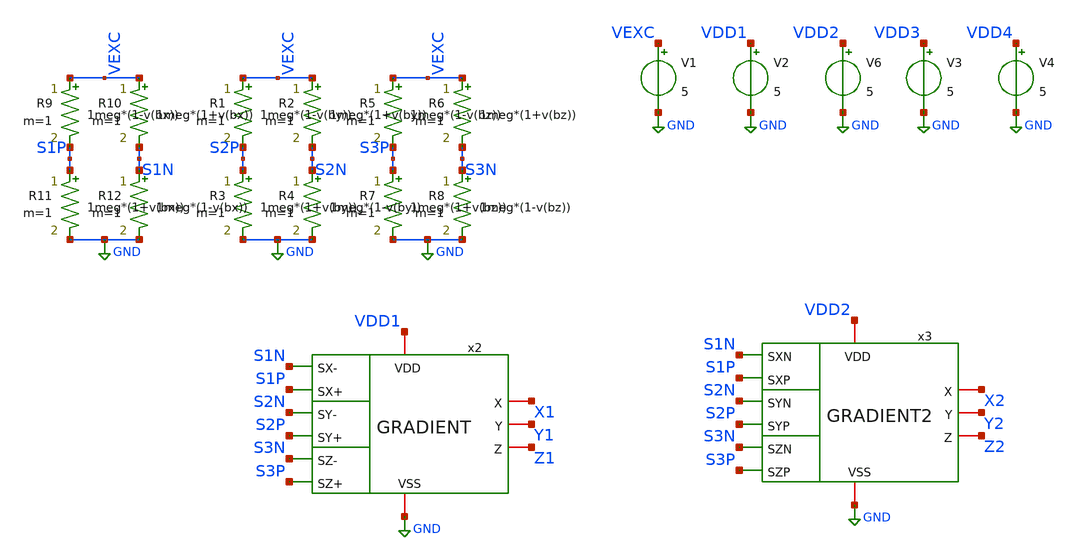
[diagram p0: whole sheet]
** sch_path: FINAL/XSCHEM/TEST_TOTAL/test_GRADIENT.sch
**.subckt test_GRADIENT
V1 VEXC GND 5
V2 VDD1 GND 5
V6 VDD2 GND 5
x2 S1N S1P VDD1 X1 S2N Y1 Z1 S2P GND S3N S3P GRADIENT
x3 S1N S1P VDD2 X2 S2N Y2 Z2 S2P GND S3N S3P GRADIENT2
R1 VEXC S2P r=' 1meg*(1-v(by)) '
R2 VEXC S2N r=' 1meg*(1+v(by)) '
R3 S2P GND r=' 1meg*(1+v(by)) '
R4 S2N GND r=' 1meg*(1-v(by)) '
V3 VDD3 GND 5
V4 VDD4 GND 5
R5 VEXC S3P r=' 1meg*(1-v(bz)) '
R6 VEXC S3N r=' 1meg*(1+v(bz)) '
R7 S3P GND r=' 1meg*(1+v(bz)) '
R8 S3N GND r=' 1meg*(1-v(bz)) '
R9 VEXC S1P r=' 1meg*(1-v(bx)) '
R10 VEXC S1N r=' 1meg*(1+v(bx)) '
R11 S1P GND r=' 1meg*(1+v(bx)) '
R12 S1N GND r=' 1meg*(1-v(bx)) '
**** begin user architecture code

.include $::180MCU_MODELS/design.ngspice
.lib $::180MCU_MODELS/sm141064.ngspice typical
.lib $::180MCU_MODELS/sm141064.ngspice cap_mim
.lib $::180MCU_MODELS/sm141064.ngspice res_typical
.lib $::180MCU_MODELS/sm141064.ngspice moscap_typical
.lib $::180MCU_MODELS/sm141064.ngspice mimcap_typical



* THE FIELD. Three components 120 degrees apart, which is what makes them sum
* to zero: the vector only changes DIRECTION, not magnitude. Sweeping
* Vang from 0 to 360 covers the whole circle, and if the chain is right each
* eje deberia ganar exactamente 120 grados: X de -60 a 60, Y de 60 a 180 y Z de
* 180 to 300. How far those three boundaries drift is the figure of the bench.
*
* v(amp) IS dR/R, with no conversion factors in between: each bridge arm is
* 1meg*(1 +- v(bx)), so the amplifier sees VEXC*v(bx) of differential signal
* and the common mode stays pinned at VEXC/2 whatever happens to
* la senal. Eso segundo no es un adorno: si el modo comun se moviera con la
* signal it would mix with these cells' common-mode sensitivity and there
* would be no way to separate the two when reading the curve.
*
* Va con fuentes B y resistencias de comportamiento, y no barriendo
* resistors, because dc takes two nested sources at most and here there are
* TWELVE resistors that must all move at once and consistently.
*
* AND A SECOND MODE, for the octant cases. The rotation above pins the three
* readings to bx+by+bz = 0, so patterns like (+,+,+) are unreachable by
* construction and this bench can only ever see three of the eight sign
* combinations. With v(sel) = 1 each reading becomes v(amp) times its own
* coefficient cx/cy/cz, so the SIGNS of those three coefficients pick the
* octant and their MAGNITUDES pick the ordering, while sweeping Vamp still
* sweeps the field inside that octant.
*
* The decoder puts out the SMALLEST axis (X = XY*XZ), so the expected answer
* at every point is argmin(cx, cy, cz) -- a truth table checkable entry by
* entry. Coefficients are given distinct magnitudes on purpose: three equal
* ones are a three-way tie with no right answer.
*
* v(sel) = 0 leaves the rotation exactly as it was: nothing above changes.
Vamp amp 0 0.02
Vang ang 0 0
Vsel sel 0 0
Vcx cx 0 1
Vcy cy 0 0
Vcz cz 0 0
Bbx bx 0 v='v(sel) > 0.5 ? v(amp)*v(cx) : v(amp)*cos( v(ang)       *3.14159265358979/180)'
Bby by 0 v='v(sel) > 0.5 ? v(amp)*v(cy) : v(amp)*cos((v(ang)-120.0)*3.14159265358979/180)'
Bbz bz 0 v='v(sel) > 0.5 ? v(amp)*v(cz) : v(amp)*cos((v(ang)+120.0)*3.14159265358979/180)'




* THE SAME TWO CHAINS, REBUILT FROM THE v2 LAYOUT BLOCKS.
* They hang off the SAME six sensor nodes as the schematic ones and each
* carries its own supply, so current draw can be compared too.
*
* La topologia es la de COMBINATION/GRADIENT.sch, copiada nodo a nodo:
*
*     amp X: S1N->INN  S1P->INP  -> SX        COMP XY: INN=SX INP=SY -> XY
*     amp Y: S2N->INN  S2P->INP  -> SY        COMP XZ: INN=SX INP=SZ -> XZ
*     amp Z: S3N->INN  S3P->INP  -> SZ        COMP YZ: INN=SY INP=SZ -> YZ
*                                             DECODER: XY XZ YZ -> X Y Z
*
* CAREFUL WITH THE PORT ORDER. xschem emits them in the order of the symbol B
* lines and magic in the order it finds them in the layout, and they do NOT agree:
* el esquematico declara OPAM VDD INN OUT INP VSS y el extraido OPAM VSS VDD OUT
* INP INN. Cablear las dos igual significa cosas distintas y no da ningun error.
* That is why the real order is written above each group, and why the files are
* the _V2_ ones produced by TEST/preparar_extraidos.sh: it renames the subcircuit
* -- both declare the same name and cannot be included together -- and normalises
* the order. Note that OPAM_LIN_flat has OUT in the middle and the others do not.
.include ../../../../layouts_v2/OPAM/mag/OPAM_V2_pex_rc.spice
.include ../../../../layouts_v2/OPAM_LIN_flat/mag/OPAM_LIN_flat_V2_pex_rc.spice
.include ../../../../layouts_v2/COMP/mag/COMP_V2_pex_rc.spice
.include ../../../../layouts_v2/DECODER/mag/DECODER_V2_pex_rc.spice

* --- G3: the G1 chain, with the v2 layout OPAM
* .subckt OPAM_V2     VSS VDD OUT INP INN
XA31 GND VDD3 SX3 S1P S1N OPAM_V2
XA32 GND VDD3 SY3 S2P S2N OPAM_V2
XA33 GND VDD3 SZ3 S3P S3N OPAM_V2
* .subckt COMP_V2     VSS VDD OUT INP INN
XC31 GND VDD3 XY3 SY3 SX3 COMP_V2
XC32 GND VDD3 XZ3 SZ3 SX3 COMP_V2
XC33 GND VDD3 YZ3 SZ3 SY3 COMP_V2
* .subckt DECODER_V2  VSS VDD YZ Z XY XZ Y X
XD3  GND VDD3 YZ3 Z3 XY3 XZ3 Y3 X3 DECODER_V2

* --- G4: the G2 chain, with the v2 layout OPAM_LIN_flat
* .subckt OPAM_LIN_flat_V2  VSS VDD INP OUT INN
XA41 GND VDD4 S1P SX4 S1N OPAM_LIN_flat_V2
XA42 GND VDD4 S2P SY4 S2N OPAM_LIN_flat_V2
XA43 GND VDD4 S3P SZ4 S3N OPAM_LIN_flat_V2
* .subckt COMP_V2     VSS VDD OUT INP INN
XC41 GND VDD4 XY4 SY4 SX4 COMP_V2
XC42 GND VDD4 XZ4 SZ4 SX4 COMP_V2
XC43 GND VDD4 YZ4 SZ4 SY4 COMP_V2
* .subckt DECODER_V2  VSS VDD YZ Z XY XZ Y X
XD4  GND VDD4 YZ4 Z4 XY4 XZ4 Y4 X4 DECODER_V2




* CAREFUL: not one brace in this text. xschem counts them to find where the
* attribute block ends and a single one inside a comment cuts it in half,
* leaving the netlist with the template 'blabla' and raising no error.
*
* This bench does NOT need a common-mode source, unlike test_comp_* and
* test_opam_*: there the input pair were two gates with no DC path to
* ground, and here the bridge itself provides it.
*
* The intermediate signals of the schematic chains come out by hierarchical
* name, v(x2.SX) and company. In the hand-rebuilt ones the nodes are
* primer nivel y se llaman SX3, XY3 y asi.
.save all
.control
* Fondo de escala de una AMR tipica: dR/R = 2 %, o sea 100 mV diferenciales.
alter Vamp = 0.02
dc Vang 0 360 0.5
wrdata ancho.txt v(X1) v(Y1) v(Z1) v(X2) v(Y2) v(Z2) v(X3) v(Y3) v(Z3) v(X4) v(Y4) v(Z4) v(x2.SX) v(x2.SY) v(x2.SZ) v(x3.SX) v(x3.SY) v(x3.SZ) v(SX3) v(SY3) v(SZ3) v(SX4) v(SY4) v(SZ4) v(x2.net1) v(x2.net2) v(x2.net3) v(x3.net1) v(x3.net2) v(x3.net3) v(XY3) v(XZ3) v(YZ3) v(XY4) v(XZ4) v(YZ4) v(S1P) v(S1N) v(S2P) v(S2N) v(S3P) v(S3N) v(VEXC)*i(V1) v(VDD1)*i(V2) v(VDD2)*i(V6) v(VDD3)*i(V3) v(VDD4)*i(V4)
* Ventana fina: dR/R = 50 ppm, o sea 250 uV diferenciales.
alter Vamp = 50u
dc Vang 0 360 0.5
wrdata fino.txt v(X1) v(Y1) v(Z1) v(X2) v(Y2) v(Z2) v(X3) v(Y3) v(Z3) v(X4) v(Y4) v(Z4) v(x2.SX) v(x2.SY) v(x2.SZ) v(x3.SX) v(x3.SY) v(x3.SZ) v(SX3) v(SY3) v(SZ3) v(SX4) v(SY4) v(SZ4) v(x2.net1) v(x2.net2) v(x2.net3) v(x3.net1) v(x3.net2) v(x3.net3) v(XY3) v(XZ3) v(YZ3) v(XY4) v(XZ4) v(YZ4) v(S1P) v(S1N) v(S2P) v(S2N) v(S3P) v(S3N) v(VEXC)*i(V1) v(VDD1)*i(V2) v(VDD2)*i(V6) v(VDD3)*i(V3) v(VDD4)*i(V4)
* --------------------------------------------------------------------------
* FIELD SWEEP. Everything above turns the field and keeps its size; these two
* do the opposite -- hold the direction and sweep the MAGNITUDE, which is the
* axis a real magnet moves along as you walk towards it.
*
* The angle is parked at 60 deg, the middle of a sector: on a boundary the
* decision is meant to be undefined and the sweep would only measure noise.
*
* AND THE SWEEP DOES NOT START AT ZERO. With Vamp = 0 the three bridges are
* identical, so the three amplifiers sit at the same output and all three
* comparators land exactly on their trip point: the operating point is not
* unique and ngspice spends the sweep in gmin stepping. Starting one step in
* costs nothing and the solution is definite everywhere.
*
* Only the linear-amplifier chain, G2 (schematic) and G4 (layout), and their
* own new files so ancho.txt and fino.txt keep the column order analizar.py
* reads.
alter Vang = 60
dc Vamp 20u 0.02 20u
wrdata campo.txt v(S1P) v(S1N) v(S2P) v(S2N) v(S3P) v(S3N)  v(x3.SX) v(x3.SY) v(x3.SZ) v(x3.net1) v(x3.net2) v(x3.net3)  v(X2) v(Y2) v(Z2)  v(SX4) v(SY4) v(SZ4) v(XY4) v(XZ4) v(YZ4)  v(X4) v(Y4) v(Z4)  v(VDD2)*i(V6) v(VDD4)*i(V4)
* And the low end on its own scale, where the offsets and the noise live.
dc Vamp 1u 1m 1u
wrdata campo_fino.txt v(S1P) v(S1N) v(S2P) v(S2N) v(S3P) v(S3N)  v(x3.SX) v(x3.SY) v(x3.SZ) v(x3.net1) v(x3.net2) v(x3.net3)  v(X2) v(Y2) v(Z2)  v(SX4) v(SY4) v(SZ4) v(XY4) v(XZ4) v(YZ4)  v(X4) v(Y4) v(Z4)  v(VDD2)*i(V6) v(VDD4)*i(V4)
* --------------------------------------------------------------------------
* OCTANT CASES. Eight sign patterns times three magnitude orderings, so
* every axis gets to be the smallest, the middle one and the largest in
* each octant: 24 cases. The coefficients are written into the file as
* its first three vectors, so each file says which case it is and no
* separate manifest can drift out of step with it.
alter Vsel = 1
* case 01: c = (+1.0, +0.6, +0.3)  ->  expected Z
alter Vcx = 1.0
alter Vcy = 0.6
alter Vcz = 0.3
dc Vamp 200u 0.02 200u
wrdata oct_01.txt v(cx) v(cy) v(cz) v(S1P) v(S1N) v(S2P) v(S2N) v(S3P) v(S3N)  v(x3.SX) v(x3.SY) v(x3.SZ) v(x3.net1) v(x3.net2) v(x3.net3)  v(X2) v(Y2) v(Z2)  v(SX4) v(SY4) v(SZ4) v(XY4) v(XZ4) v(YZ4)  v(X4) v(Y4) v(Z4)
* case 02: c = (+0.3, +1.0, +0.6)  ->  expected X
alter Vcx = 0.3
alter Vcy = 1.0
alter Vcz = 0.6
dc Vamp 200u 0.02 200u
wrdata oct_02.txt v(cx) v(cy) v(cz) v(S1P) v(S1N) v(S2P) v(S2N) v(S3P) v(S3N)  v(x3.SX) v(x3.SY) v(x3.SZ) v(x3.net1) v(x3.net2) v(x3.net3)  v(X2) v(Y2) v(Z2)  v(SX4) v(SY4) v(SZ4) v(XY4) v(XZ4) v(YZ4)  v(X4) v(Y4) v(Z4)
* case 03: c = (+0.6, +0.3, +1.0)  ->  expected Y
alter Vcx = 0.6
alter Vcy = 0.3
alter Vcz = 1.0
dc Vamp 200u 0.02 200u
wrdata oct_03.txt v(cx) v(cy) v(cz) v(S1P) v(S1N) v(S2P) v(S2N) v(S3P) v(S3N)  v(x3.SX) v(x3.SY) v(x3.SZ) v(x3.net1) v(x3.net2) v(x3.net3)  v(X2) v(Y2) v(Z2)  v(SX4) v(SY4) v(SZ4) v(XY4) v(XZ4) v(YZ4)  v(X4) v(Y4) v(Z4)
* case 04: c = (+1.0, +0.6, -0.3)  ->  expected Z
alter Vcx = 1.0
alter Vcy = 0.6
alter Vcz = -0.3
dc Vamp 200u 0.02 200u
wrdata oct_04.txt v(cx) v(cy) v(cz) v(S1P) v(S1N) v(S2P) v(S2N) v(S3P) v(S3N)  v(x3.SX) v(x3.SY) v(x3.SZ) v(x3.net1) v(x3.net2) v(x3.net3)  v(X2) v(Y2) v(Z2)  v(SX4) v(SY4) v(SZ4) v(XY4) v(XZ4) v(YZ4)  v(X4) v(Y4) v(Z4)
* case 05: c = (+0.3, +1.0, -0.6)  ->  expected Z
alter Vcx = 0.3
alter Vcy = 1.0
alter Vcz = -0.6
dc Vamp 200u 0.02 200u
wrdata oct_05.txt v(cx) v(cy) v(cz) v(S1P) v(S1N) v(S2P) v(S2N) v(S3P) v(S3N)  v(x3.SX) v(x3.SY) v(x3.SZ) v(x3.net1) v(x3.net2) v(x3.net3)  v(X2) v(Y2) v(Z2)  v(SX4) v(SY4) v(SZ4) v(XY4) v(XZ4) v(YZ4)  v(X4) v(Y4) v(Z4)
* case 06: c = (+0.6, +0.3, -1.0)  ->  expected Z
alter Vcx = 0.6
alter Vcy = 0.3
alter Vcz = -1.0
dc Vamp 200u 0.02 200u
wrdata oct_06.txt v(cx) v(cy) v(cz) v(S1P) v(S1N) v(S2P) v(S2N) v(S3P) v(S3N)  v(x3.SX) v(x3.SY) v(x3.SZ) v(x3.net1) v(x3.net2) v(x3.net3)  v(X2) v(Y2) v(Z2)  v(SX4) v(SY4) v(SZ4) v(XY4) v(XZ4) v(YZ4)  v(X4) v(Y4) v(Z4)
* case 07: c = (+1.0, -0.6, +0.3)  ->  expected Y
alter Vcx = 1.0
alter Vcy = -0.6
alter Vcz = 0.3
dc Vamp 200u 0.02 200u
wrdata oct_07.txt v(cx) v(cy) v(cz) v(S1P) v(S1N) v(S2P) v(S2N) v(S3P) v(S3N)  v(x3.SX) v(x3.SY) v(x3.SZ) v(x3.net1) v(x3.net2) v(x3.net3)  v(X2) v(Y2) v(Z2)  v(SX4) v(SY4) v(SZ4) v(XY4) v(XZ4) v(YZ4)  v(X4) v(Y4) v(Z4)
* case 08: c = (+0.3, -1.0, +0.6)  ->  expected Y
alter Vcx = 0.3
alter Vcy = -1.0
alter Vcz = 0.6
dc Vamp 200u 0.02 200u
wrdata oct_08.txt v(cx) v(cy) v(cz) v(S1P) v(S1N) v(S2P) v(S2N) v(S3P) v(S3N)  v(x3.SX) v(x3.SY) v(x3.SZ) v(x3.net1) v(x3.net2) v(x3.net3)  v(X2) v(Y2) v(Z2)  v(SX4) v(SY4) v(SZ4) v(XY4) v(XZ4) v(YZ4)  v(X4) v(Y4) v(Z4)
* case 09: c = (+0.6, -0.3, +1.0)  ->  expected Y
alter Vcx = 0.6
alter Vcy = -0.3
alter Vcz = 1.0
dc Vamp 200u 0.02 200u
wrdata oct_09.txt v(cx) v(cy) v(cz) v(S1P) v(S1N) v(S2P) v(S2N) v(S3P) v(S3N)  v(x3.SX) v(x3.SY) v(x3.SZ) v(x3.net1) v(x3.net2) v(x3.net3)  v(X2) v(Y2) v(Z2)  v(SX4) v(SY4) v(SZ4) v(XY4) v(XZ4) v(YZ4)  v(X4) v(Y4) v(Z4)
* case 10: c = (+1.0, -0.6, -0.3)  ->  expected Y
alter Vcx = 1.0
alter Vcy = -0.6
alter Vcz = -0.3
dc Vamp 200u 0.02 200u
wrdata oct_10.txt v(cx) v(cy) v(cz) v(S1P) v(S1N) v(S2P) v(S2N) v(S3P) v(S3N)  v(x3.SX) v(x3.SY) v(x3.SZ) v(x3.net1) v(x3.net2) v(x3.net3)  v(X2) v(Y2) v(Z2)  v(SX4) v(SY4) v(SZ4) v(XY4) v(XZ4) v(YZ4)  v(X4) v(Y4) v(Z4)
* case 11: c = (+0.3, -1.0, -0.6)  ->  expected Y
alter Vcx = 0.3
alter Vcy = -1.0
alter Vcz = -0.6
dc Vamp 200u 0.02 200u
wrdata oct_11.txt v(cx) v(cy) v(cz) v(S1P) v(S1N) v(S2P) v(S2N) v(S3P) v(S3N)  v(x3.SX) v(x3.SY) v(x3.SZ) v(x3.net1) v(x3.net2) v(x3.net3)  v(X2) v(Y2) v(Z2)  v(SX4) v(SY4) v(SZ4) v(XY4) v(XZ4) v(YZ4)  v(X4) v(Y4) v(Z4)
* case 12: c = (+0.6, -0.3, -1.0)  ->  expected Z
alter Vcx = 0.6
alter Vcy = -0.3
alter Vcz = -1.0
dc Vamp 200u 0.02 200u
wrdata oct_12.txt v(cx) v(cy) v(cz) v(S1P) v(S1N) v(S2P) v(S2N) v(S3P) v(S3N)  v(x3.SX) v(x3.SY) v(x3.SZ) v(x3.net1) v(x3.net2) v(x3.net3)  v(X2) v(Y2) v(Z2)  v(SX4) v(SY4) v(SZ4) v(XY4) v(XZ4) v(YZ4)  v(X4) v(Y4) v(Z4)
* case 13: c = (-1.0, +0.6, +0.3)  ->  expected X
alter Vcx = -1.0
alter Vcy = 0.6
alter Vcz = 0.3
dc Vamp 200u 0.02 200u
wrdata oct_13.txt v(cx) v(cy) v(cz) v(S1P) v(S1N) v(S2P) v(S2N) v(S3P) v(S3N)  v(x3.SX) v(x3.SY) v(x3.SZ) v(x3.net1) v(x3.net2) v(x3.net3)  v(X2) v(Y2) v(Z2)  v(SX4) v(SY4) v(SZ4) v(XY4) v(XZ4) v(YZ4)  v(X4) v(Y4) v(Z4)
* case 14: c = (-0.3, +1.0, +0.6)  ->  expected X
alter Vcx = -0.3
alter Vcy = 1.0
alter Vcz = 0.6
dc Vamp 200u 0.02 200u
wrdata oct_14.txt v(cx) v(cy) v(cz) v(S1P) v(S1N) v(S2P) v(S2N) v(S3P) v(S3N)  v(x3.SX) v(x3.SY) v(x3.SZ) v(x3.net1) v(x3.net2) v(x3.net3)  v(X2) v(Y2) v(Z2)  v(SX4) v(SY4) v(SZ4) v(XY4) v(XZ4) v(YZ4)  v(X4) v(Y4) v(Z4)
* case 15: c = (-0.6, +0.3, +1.0)  ->  expected X
alter Vcx = -0.6
alter Vcy = 0.3
alter Vcz = 1.0
dc Vamp 200u 0.02 200u
wrdata oct_15.txt v(cx) v(cy) v(cz) v(S1P) v(S1N) v(S2P) v(S2N) v(S3P) v(S3N)  v(x3.SX) v(x3.SY) v(x3.SZ) v(x3.net1) v(x3.net2) v(x3.net3)  v(X2) v(Y2) v(Z2)  v(SX4) v(SY4) v(SZ4) v(XY4) v(XZ4) v(YZ4)  v(X4) v(Y4) v(Z4)
* case 16: c = (-1.0, +0.6, -0.3)  ->  expected X
alter Vcx = -1.0
alter Vcy = 0.6
alter Vcz = -0.3
dc Vamp 200u 0.02 200u
wrdata oct_16.txt v(cx) v(cy) v(cz) v(S1P) v(S1N) v(S2P) v(S2N) v(S3P) v(S3N)  v(x3.SX) v(x3.SY) v(x3.SZ) v(x3.net1) v(x3.net2) v(x3.net3)  v(X2) v(Y2) v(Z2)  v(SX4) v(SY4) v(SZ4) v(XY4) v(XZ4) v(YZ4)  v(X4) v(Y4) v(Z4)
* case 17: c = (-0.3, +1.0, -0.6)  ->  expected Z
alter Vcx = -0.3
alter Vcy = 1.0
alter Vcz = -0.6
dc Vamp 200u 0.02 200u
wrdata oct_17.txt v(cx) v(cy) v(cz) v(S1P) v(S1N) v(S2P) v(S2N) v(S3P) v(S3N)  v(x3.SX) v(x3.SY) v(x3.SZ) v(x3.net1) v(x3.net2) v(x3.net3)  v(X2) v(Y2) v(Z2)  v(SX4) v(SY4) v(SZ4) v(XY4) v(XZ4) v(YZ4)  v(X4) v(Y4) v(Z4)
* case 18: c = (-0.6, +0.3, -1.0)  ->  expected Z
alter Vcx = -0.6
alter Vcy = 0.3
alter Vcz = -1.0
dc Vamp 200u 0.02 200u
wrdata oct_18.txt v(cx) v(cy) v(cz) v(S1P) v(S1N) v(S2P) v(S2N) v(S3P) v(S3N)  v(x3.SX) v(x3.SY) v(x3.SZ) v(x3.net1) v(x3.net2) v(x3.net3)  v(X2) v(Y2) v(Z2)  v(SX4) v(SY4) v(SZ4) v(XY4) v(XZ4) v(YZ4)  v(X4) v(Y4) v(Z4)
* case 19: c = (-1.0, -0.6, +0.3)  ->  expected X
alter Vcx = -1.0
alter Vcy = -0.6
alter Vcz = 0.3
dc Vamp 200u 0.02 200u
wrdata oct_19.txt v(cx) v(cy) v(cz) v(S1P) v(S1N) v(S2P) v(S2N) v(S3P) v(S3N)  v(x3.SX) v(x3.SY) v(x3.SZ) v(x3.net1) v(x3.net2) v(x3.net3)  v(X2) v(Y2) v(Z2)  v(SX4) v(SY4) v(SZ4) v(XY4) v(XZ4) v(YZ4)  v(X4) v(Y4) v(Z4)
* case 20: c = (-0.3, -1.0, +0.6)  ->  expected Y
alter Vcx = -0.3
alter Vcy = -1.0
alter Vcz = 0.6
dc Vamp 200u 0.02 200u
wrdata oct_20.txt v(cx) v(cy) v(cz) v(S1P) v(S1N) v(S2P) v(S2N) v(S3P) v(S3N)  v(x3.SX) v(x3.SY) v(x3.SZ) v(x3.net1) v(x3.net2) v(x3.net3)  v(X2) v(Y2) v(Z2)  v(SX4) v(SY4) v(SZ4) v(XY4) v(XZ4) v(YZ4)  v(X4) v(Y4) v(Z4)
* case 21: c = (-0.6, -0.3, +1.0)  ->  expected X
alter Vcx = -0.6
alter Vcy = -0.3
alter Vcz = 1.0
dc Vamp 200u 0.02 200u
wrdata oct_21.txt v(cx) v(cy) v(cz) v(S1P) v(S1N) v(S2P) v(S2N) v(S3P) v(S3N)  v(x3.SX) v(x3.SY) v(x3.SZ) v(x3.net1) v(x3.net2) v(x3.net3)  v(X2) v(Y2) v(Z2)  v(SX4) v(SY4) v(SZ4) v(XY4) v(XZ4) v(YZ4)  v(X4) v(Y4) v(Z4)
* case 22: c = (-1.0, -0.6, -0.3)  ->  expected X
alter Vcx = -1.0
alter Vcy = -0.6
alter Vcz = -0.3
dc Vamp 200u 0.02 200u
wrdata oct_22.txt v(cx) v(cy) v(cz) v(S1P) v(S1N) v(S2P) v(S2N) v(S3P) v(S3N)  v(x3.SX) v(x3.SY) v(x3.SZ) v(x3.net1) v(x3.net2) v(x3.net3)  v(X2) v(Y2) v(Z2)  v(SX4) v(SY4) v(SZ4) v(XY4) v(XZ4) v(YZ4)  v(X4) v(Y4) v(Z4)
* case 23: c = (-0.3, -1.0, -0.6)  ->  expected Y
alter Vcx = -0.3
alter Vcy = -1.0
alter Vcz = -0.6
dc Vamp 200u 0.02 200u
wrdata oct_23.txt v(cx) v(cy) v(cz) v(S1P) v(S1N) v(S2P) v(S2N) v(S3P) v(S3N)  v(x3.SX) v(x3.SY) v(x3.SZ) v(x3.net1) v(x3.net2) v(x3.net3)  v(X2) v(Y2) v(Z2)  v(SX4) v(SY4) v(SZ4) v(XY4) v(XZ4) v(YZ4)  v(X4) v(Y4) v(Z4)
* case 24: c = (-0.6, -0.3, -1.0)  ->  expected Z
alter Vcx = -0.6
alter Vcy = -0.3
alter Vcz = -1.0
dc Vamp 200u 0.02 200u
wrdata oct_24.txt v(cx) v(cy) v(cz) v(S1P) v(S1N) v(S2P) v(S2N) v(S3P) v(S3N)  v(x3.SX) v(x3.SY) v(x3.SZ) v(x3.net1) v(x3.net2) v(x3.net3)  v(X2) v(Y2) v(Z2)  v(SX4) v(SY4) v(SZ4) v(XY4) v(XZ4) v(YZ4)  v(X4) v(Y4) v(Z4)
* --------------------------------------------------------------------------
* LIMIT CASES. The octant block above says the block is 94.8 % correct and
* leaves it there. That number is the average of a test where NINE of its
* twenty-four cases sit in the same corner, so it moves when the case list
* moves and says nothing about the circuit. This block measures the corner.
*
* WHAT THE CORNER IS. The decoder puts out the SMALLEST reading, so two of the
* three contend for it and the answer holds only while the amplifier still
* separates those two. Measured on the octant runs, the amplifier rests at
* 0.72 V with 4.24 V of room upward and 0.68 V downward -- SIX TIMES less --
* so a contending pair heading DOWN pins against its rail six times sooner
* than the same pair heading up. That, and not the sign of the octant, is what
* the 94.8 % is made of.
*
* Three families, same margin d between the two contenders, the third reading
* parked where it cannot compete:
*
*   A  pair DOWN, full scale   c = (-1.0, -1.0+d, +0.3)   expected X
*   B  pair DOWN, half scale   c = (-0.5, -0.5+d, +1.0)   expected X
*   C  pair UP,   half scale   c = (+0.5, +0.5+d, +1.0)   expected X
*
* A against B separates the RAIL from the SIZE. B against C separates the two
* rails at equal size, which is the six-to-one asymmetry on its own. Four
* margins each: twelve runs, and the answer is always X, so a flipped output
* is a failure and nothing else.
*
* Files are `lim_NN.txt` and NOT `oct_NN.txt` on purpose: `figuras_octantes.py`
* globs `oct_*.txt`, and a file of a different meaning landing in that glob
* would be read as a ninth octant and would quietly move a published number.
* limit 01: family A, d = 0.05, pair down at 1.0  ->  expected X
alter Vcx = -1.0
alter Vcy = -0.95
alter Vcz = 0.3
dc Vamp 200u 0.02 200u
wrdata lim_01.txt v(cx) v(cy) v(cz) v(S1P) v(S1N) v(S2P) v(S2N) v(S3P) v(S3N)  v(x3.SX) v(x3.SY) v(x3.SZ) v(x3.net1) v(x3.net2) v(x3.net3)  v(X2) v(Y2) v(Z2)  v(SX4) v(SY4) v(SZ4) v(XY4) v(XZ4) v(YZ4)  v(X4) v(Y4) v(Z4)
* limit 02: family A, d = 0.10, pair down at 1.0  ->  expected X
alter Vcx = -1.0
alter Vcy = -0.90
alter Vcz = 0.3
dc Vamp 200u 0.02 200u
wrdata lim_02.txt v(cx) v(cy) v(cz) v(S1P) v(S1N) v(S2P) v(S2N) v(S3P) v(S3N)  v(x3.SX) v(x3.SY) v(x3.SZ) v(x3.net1) v(x3.net2) v(x3.net3)  v(X2) v(Y2) v(Z2)  v(SX4) v(SY4) v(SZ4) v(XY4) v(XZ4) v(YZ4)  v(X4) v(Y4) v(Z4)
* limit 03: family A, d = 0.20, pair down at 1.0  ->  expected X
alter Vcx = -1.0
alter Vcy = -0.80
alter Vcz = 0.3
dc Vamp 200u 0.02 200u
wrdata lim_03.txt v(cx) v(cy) v(cz) v(S1P) v(S1N) v(S2P) v(S2N) v(S3P) v(S3N)  v(x3.SX) v(x3.SY) v(x3.SZ) v(x3.net1) v(x3.net2) v(x3.net3)  v(X2) v(Y2) v(Z2)  v(SX4) v(SY4) v(SZ4) v(XY4) v(XZ4) v(YZ4)  v(X4) v(Y4) v(Z4)
* limit 04: family A, d = 0.40, pair down at 1.0  ->  expected X
alter Vcx = -1.0
alter Vcy = -0.60
alter Vcz = 0.3
dc Vamp 200u 0.02 200u
wrdata lim_04.txt v(cx) v(cy) v(cz) v(S1P) v(S1N) v(S2P) v(S2N) v(S3P) v(S3N)  v(x3.SX) v(x3.SY) v(x3.SZ) v(x3.net1) v(x3.net2) v(x3.net3)  v(X2) v(Y2) v(Z2)  v(SX4) v(SY4) v(SZ4) v(XY4) v(XZ4) v(YZ4)  v(X4) v(Y4) v(Z4)
* limit 05: family B, d = 0.05, pair down at 0.5  ->  expected X
alter Vcx = -0.5
alter Vcy = -0.45
alter Vcz = 1.0
dc Vamp 200u 0.02 200u
wrdata lim_05.txt v(cx) v(cy) v(cz) v(S1P) v(S1N) v(S2P) v(S2N) v(S3P) v(S3N)  v(x3.SX) v(x3.SY) v(x3.SZ) v(x3.net1) v(x3.net2) v(x3.net3)  v(X2) v(Y2) v(Z2)  v(SX4) v(SY4) v(SZ4) v(XY4) v(XZ4) v(YZ4)  v(X4) v(Y4) v(Z4)
* limit 06: family B, d = 0.10, pair down at 0.5  ->  expected X
alter Vcx = -0.5
alter Vcy = -0.40
alter Vcz = 1.0
dc Vamp 200u 0.02 200u
wrdata lim_06.txt v(cx) v(cy) v(cz) v(S1P) v(S1N) v(S2P) v(S2N) v(S3P) v(S3N)  v(x3.SX) v(x3.SY) v(x3.SZ) v(x3.net1) v(x3.net2) v(x3.net3)  v(X2) v(Y2) v(Z2)  v(SX4) v(SY4) v(SZ4) v(XY4) v(XZ4) v(YZ4)  v(X4) v(Y4) v(Z4)
* limit 07: family B, d = 0.20, pair down at 0.5  ->  expected X
alter Vcx = -0.5
alter Vcy = -0.30
alter Vcz = 1.0
dc Vamp 200u 0.02 200u
wrdata lim_07.txt v(cx) v(cy) v(cz) v(S1P) v(S1N) v(S2P) v(S2N) v(S3P) v(S3N)  v(x3.SX) v(x3.SY) v(x3.SZ) v(x3.net1) v(x3.net2) v(x3.net3)  v(X2) v(Y2) v(Z2)  v(SX4) v(SY4) v(SZ4) v(XY4) v(XZ4) v(YZ4)  v(X4) v(Y4) v(Z4)
* limit 08: family B, d = 0.40, pair down at 0.5  ->  expected X
alter Vcx = -0.5
alter Vcy = -0.10
alter Vcz = 1.0
dc Vamp 200u 0.02 200u
wrdata lim_08.txt v(cx) v(cy) v(cz) v(S1P) v(S1N) v(S2P) v(S2N) v(S3P) v(S3N)  v(x3.SX) v(x3.SY) v(x3.SZ) v(x3.net1) v(x3.net2) v(x3.net3)  v(X2) v(Y2) v(Z2)  v(SX4) v(SY4) v(SZ4) v(XY4) v(XZ4) v(YZ4)  v(X4) v(Y4) v(Z4)
* limit 09: family C, d = 0.05, pair up at 0.5  ->  expected X
alter Vcx = 0.5
alter Vcy = 0.55
alter Vcz = 1.0
dc Vamp 200u 0.02 200u
wrdata lim_09.txt v(cx) v(cy) v(cz) v(S1P) v(S1N) v(S2P) v(S2N) v(S3P) v(S3N)  v(x3.SX) v(x3.SY) v(x3.SZ) v(x3.net1) v(x3.net2) v(x3.net3)  v(X2) v(Y2) v(Z2)  v(SX4) v(SY4) v(SZ4) v(XY4) v(XZ4) v(YZ4)  v(X4) v(Y4) v(Z4)
* limit 10: family C, d = 0.10, pair up at 0.5  ->  expected X
alter Vcx = 0.5
alter Vcy = 0.60
alter Vcz = 1.0
dc Vamp 200u 0.02 200u
wrdata lim_10.txt v(cx) v(cy) v(cz) v(S1P) v(S1N) v(S2P) v(S2N) v(S3P) v(S3N)  v(x3.SX) v(x3.SY) v(x3.SZ) v(x3.net1) v(x3.net2) v(x3.net3)  v(X2) v(Y2) v(Z2)  v(SX4) v(SY4) v(SZ4) v(XY4) v(XZ4) v(YZ4)  v(X4) v(Y4) v(Z4)
* limit 11: family C, d = 0.20, pair up at 0.5  ->  expected X
alter Vcx = 0.5
alter Vcy = 0.70
alter Vcz = 1.0
dc Vamp 200u 0.02 200u
wrdata lim_11.txt v(cx) v(cy) v(cz) v(S1P) v(S1N) v(S2P) v(S2N) v(S3P) v(S3N)  v(x3.SX) v(x3.SY) v(x3.SZ) v(x3.net1) v(x3.net2) v(x3.net3)  v(X2) v(Y2) v(Z2)  v(SX4) v(SY4) v(SZ4) v(XY4) v(XZ4) v(YZ4)  v(X4) v(Y4) v(Z4)
* limit 12: family C, d = 0.40, pair up at 0.5  ->  expected X
alter Vcx = 0.5
alter Vcy = 0.90
alter Vcz = 1.0
dc Vamp 200u 0.02 200u
wrdata lim_12.txt v(cx) v(cy) v(cz) v(S1P) v(S1N) v(S2P) v(S2N) v(S3P) v(S3N)  v(x3.SX) v(x3.SY) v(x3.SZ) v(x3.net1) v(x3.net2) v(x3.net3)  v(X2) v(Y2) v(Z2)  v(SX4) v(SY4) v(SZ4) v(XY4) v(XZ4) v(YZ4)  v(X4) v(Y4) v(Z4)
alter Vsel = 0
.endc


**** end user architecture code
**.ends
.GLOBAL GND
.end
